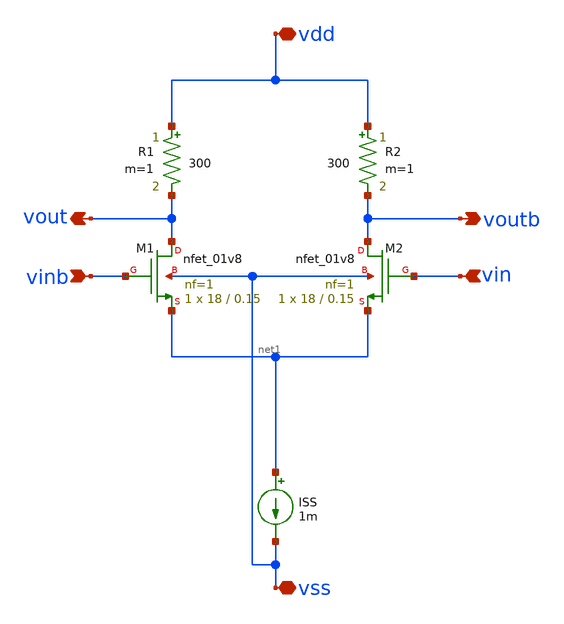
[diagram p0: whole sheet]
** sch_path: xschem/cml_inverter.sch
**.subckt cml_inverter vinb vin vdd vss vout voutb
*.ipin vinb
*.ipin vin
*.iopin vdd
*.iopin vss
*.opin vout
*.opin voutb
ISS net1 vss 1m
R1 vdd vout 300 m=1
R2 vdd voutb 300 m=1
XM1 vout vinb net1 vss sky130_fd_pr__nfet_01v8 L=0.15 W=18 nf=1 ad='int((nf+1)/2) * W/nf * 0.29' as='int((nf+2)/2) * W/nf * 0.29'
+ pd='2*int((nf+1)/2) * (W/nf + 0.29)' ps='2*int((nf+2)/2) * (W/nf + 0.29)' nrd='0.29 / W' nrs='0.29 / W'
+ sa=0 sb=0 sd=0 mult=1 m=1
XM2 voutb vin net1 vss sky130_fd_pr__nfet_01v8 L=0.15 W=18 nf=1 ad='int((nf+1)/2) * W/nf * 0.29' as='int((nf+2)/2) * W/nf * 0.29'
+ pd='2*int((nf+1)/2) * (W/nf + 0.29)' ps='2*int((nf+2)/2) * (W/nf + 0.29)' nrd='0.29 / W' nrs='0.29 / W'
+ sa=0 sb=0 sd=0 mult=1 m=1
**.ends
.end
